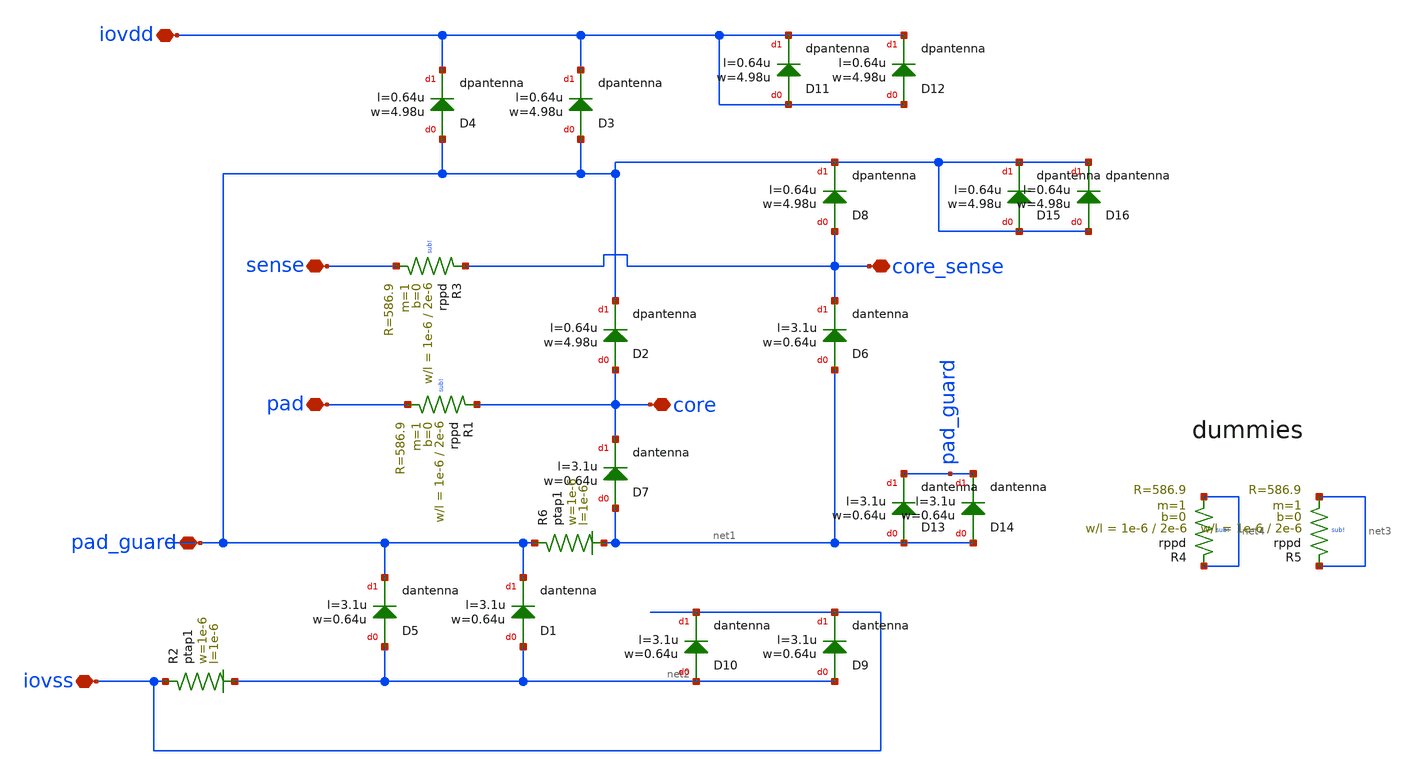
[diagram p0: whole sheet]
** sch_path: trident_test_structures/design_data/xschem/IOPadAnalogGuardLayerSense/secondary_protection_guard_layer_sense.sch
**.subckt secondary_protection_guard_layer_sense iovss iovdd pad pad_guard core sense core_sense
*.iopin iovss
*.iopin iovdd
*.iopin pad
*.iopin pad_guard
*.iopin core
*.iopin sense
*.iopin core_sense
XR1 core pad sub! rppd w=1e-6 l=2e-6 m=1 b=0 mm_ok=1
XD7 net1 core dantenna l=3.1u w=0.64u
XD1 net2 pad_guard dantenna l=3.1u w=0.64u
XD2 core pad_guard dpantenna l=0.64u w=4.98u
XD3 pad_guard iovdd dpantenna l=0.64u w=4.98u
XR2 iovss net2 ptap1 R=196 w=1e-6 l=1e-6
XD4 pad_guard iovdd dpantenna l=0.64u w=4.98u
XD5 net2 pad_guard dantenna l=3.1u w=0.64u
XR3 core_sense sense sub! rppd w=1e-6 l=2e-6 m=1 b=0 mm_ok=1
XD6 net1 core_sense dantenna l=3.1u w=0.64u
XD8 core_sense pad_guard dpantenna l=0.64u w=4.98u
XR4 net4 net4 sub! rppd w=1e-6 l=2e-6 m=1 b=0 mm_ok=1
XR5 net3 net3 sub! rppd w=1e-6 l=2e-6 m=1 b=0 mm_ok=1
XD11 iovdd iovdd dpantenna l=0.64u w=4.98u
XD12 iovdd iovdd dpantenna l=0.64u w=4.98u
XD9 net2 iovss dantenna l=3.1u w=0.64u
XD10 net2 iovss dantenna l=3.1u w=0.64u
XD13 net1 pad_guard dantenna l=3.1u w=0.64u
XD14 net1 pad_guard dantenna l=3.1u w=0.64u
XD15 pad_guard pad_guard dpantenna l=0.64u w=4.98u
XD16 pad_guard pad_guard dpantenna l=0.64u w=4.98u
XR6 pad_guard net1 ptap1 R=196 w=1e-6 l=1e-6
**.ends
.end
